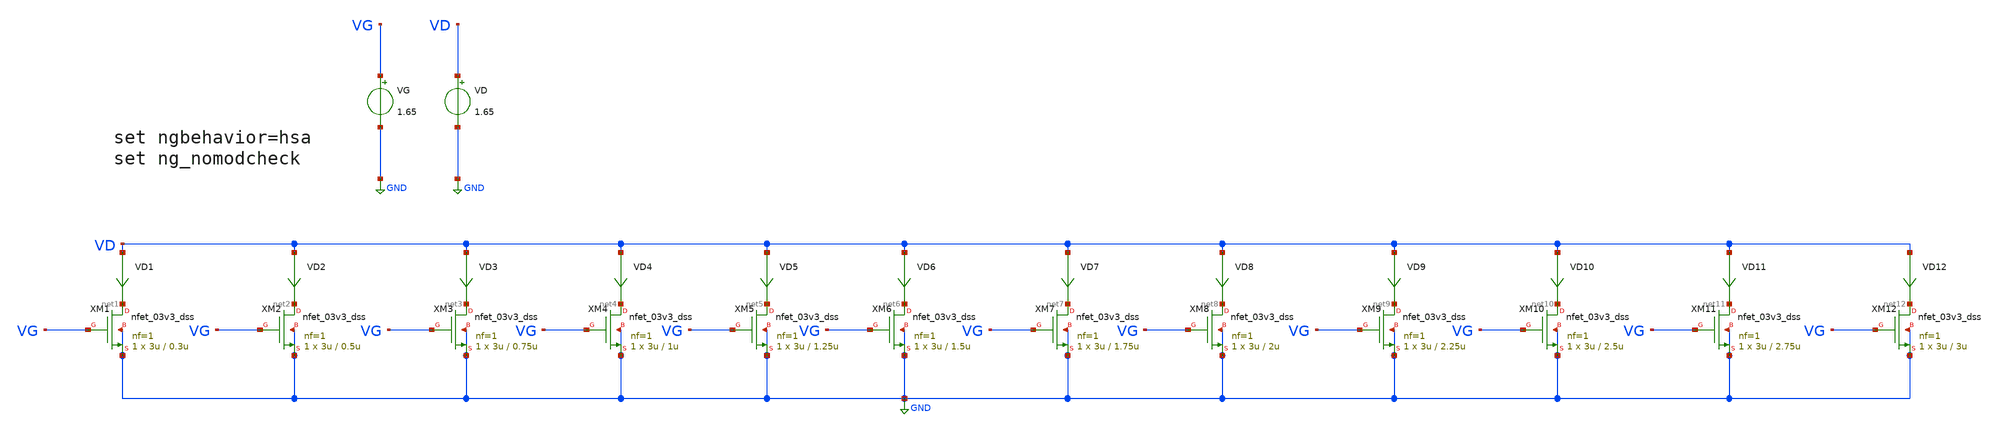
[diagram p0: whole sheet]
** sch_path: Design-Files/gmid_nmos_03v3_dss.sch
**.subckt gmid_nmos_03v3_dss
VG VG GND 1.65
VD VD GND 1.65
VD1 VD net1 0
.save i(vd1)
VD2 VD net2 0
.save i(vd2)
VD3 VD net3 0
.save i(vd3)
VD4 VD net4 0
.save i(vd4)
VD5 VD net5 0
.save i(vd5)
VD6 VD net6 0
.save i(vd6)
VD7 VD net7 0
.save i(vd7)
VD8 VD net8 0
.save i(vd8)
VD9 VD net9 0
.save i(vd9)
VD10 VD net10 0
.save i(vd10)
VD11 VD net11 0
.save i(vd11)
VD12 VD net12 0
.save i(vd12)
XM1 net1 VG GND GND nfet_03v3_dss L=0.3u W=3u nf=1 ad='int((nf+1)/2) * W/nf * 0.18u' as='int((nf+2)/2) * W/nf * 0.18u'
+ pd='2*int((nf+1)/2) * (W/nf + 0.18u)' ps='2*int((nf+2)/2) * (W/nf + 0.18u)' nrd='0.18u / W' nrs='0.18u / W'
+ sa=0 sb=0 sd=0 m=1
XM2 net2 VG GND GND nfet_03v3_dss L=0.5u W=3u nf=1 ad='int((nf+1)/2) * W/nf * 0.18u' as='int((nf+2)/2) * W/nf * 0.18u'
+ pd='2*int((nf+1)/2) * (W/nf + 0.18u)' ps='2*int((nf+2)/2) * (W/nf + 0.18u)' nrd='0.18u / W' nrs='0.18u / W'
+ sa=0 sb=0 sd=0 m=1
XM3 net3 VG GND GND nfet_03v3_dss L=0.75u W=3u nf=1 ad='int((nf+1)/2) * W/nf * 0.18u' as='int((nf+2)/2) * W/nf * 0.18u'
+ pd='2*int((nf+1)/2) * (W/nf + 0.18u)' ps='2*int((nf+2)/2) * (W/nf + 0.18u)' nrd='0.18u / W' nrs='0.18u / W'
+ sa=0 sb=0 sd=0 m=1
XM4 net4 VG GND GND nfet_03v3_dss L=1u W=3u nf=1 ad='int((nf+1)/2) * W/nf * 0.18u' as='int((nf+2)/2) * W/nf * 0.18u'
+ pd='2*int((nf+1)/2) * (W/nf + 0.18u)' ps='2*int((nf+2)/2) * (W/nf + 0.18u)' nrd='0.18u / W' nrs='0.18u / W'
+ sa=0 sb=0 sd=0 m=1
XM5 net5 VG GND GND nfet_03v3_dss L=1.25u W=3u nf=1 ad='int((nf+1)/2) * W/nf * 0.18u' as='int((nf+2)/2) * W/nf * 0.18u'
+ pd='2*int((nf+1)/2) * (W/nf + 0.18u)' ps='2*int((nf+2)/2) * (W/nf + 0.18u)' nrd='0.18u / W' nrs='0.18u / W'
+ sa=0 sb=0 sd=0 m=1
XM6 net6 VG GND GND nfet_03v3_dss L=1.5u W=3u nf=1 ad='int((nf+1)/2) * W/nf * 0.18u' as='int((nf+2)/2) * W/nf * 0.18u'
+ pd='2*int((nf+1)/2) * (W/nf + 0.18u)' ps='2*int((nf+2)/2) * (W/nf + 0.18u)' nrd='0.18u / W' nrs='0.18u / W'
+ sa=0 sb=0 sd=0 m=1
XM7 net7 VG GND GND nfet_03v3_dss L=1.75u W=3u nf=1 ad='int((nf+1)/2) * W/nf * 0.18u' as='int((nf+2)/2) * W/nf * 0.18u'
+ pd='2*int((nf+1)/2) * (W/nf + 0.18u)' ps='2*int((nf+2)/2) * (W/nf + 0.18u)' nrd='0.18u / W' nrs='0.18u / W'
+ sa=0 sb=0 sd=0 m=1
XM8 net8 VG GND GND nfet_03v3_dss L=2u W=3u nf=1 ad='int((nf+1)/2) * W/nf * 0.18u' as='int((nf+2)/2) * W/nf * 0.18u'
+ pd='2*int((nf+1)/2) * (W/nf + 0.18u)' ps='2*int((nf+2)/2) * (W/nf + 0.18u)' nrd='0.18u / W' nrs='0.18u / W'
+ sa=0 sb=0 sd=0 m=1
XM9 net9 VG GND GND nfet_03v3_dss L=2.25u W=3u nf=1 ad='int((nf+1)/2) * W/nf * 0.18u' as='int((nf+2)/2) * W/nf * 0.18u'
+ pd='2*int((nf+1)/2) * (W/nf + 0.18u)' ps='2*int((nf+2)/2) * (W/nf + 0.18u)' nrd='0.18u / W' nrs='0.18u / W'
+ sa=0 sb=0 sd=0 m=1
XM10 net10 VG GND GND nfet_03v3_dss L=2.5u W=3u nf=1 ad='int((nf+1)/2) * W/nf * 0.18u' as='int((nf+2)/2) * W/nf * 0.18u'
+ pd='2*int((nf+1)/2) * (W/nf + 0.18u)' ps='2*int((nf+2)/2) * (W/nf + 0.18u)' nrd='0.18u / W' nrs='0.18u / W'
+ sa=0 sb=0 sd=0 m=1
XM11 net11 VG GND GND nfet_03v3_dss L=2.75u W=3u nf=1 ad='int((nf+1)/2) * W/nf * 0.18u' as='int((nf+2)/2) * W/nf * 0.18u'
+ pd='2*int((nf+1)/2) * (W/nf + 0.18u)' ps='2*int((nf+2)/2) * (W/nf + 0.18u)' nrd='0.18u / W' nrs='0.18u / W'
+ sa=0 sb=0 sd=0 m=1
XM12 net12 VG GND GND nfet_03v3_dss L=3u W=3u nf=1 ad='int((nf+1)/2) * W/nf * 0.18u' as='int((nf+2)/2) * W/nf * 0.18u'
+ pd='2*int((nf+1)/2) * (W/nf + 0.18u)' ps='2*int((nf+2)/2) * (W/nf + 0.18u)' nrd='0.18u / W' nrs='0.18u / W'
+ sa=0 sb=0 sd=0 m=1
**** begin user architecture code


* ngspice commands
.option wnflag=1
.option .savecurrents
.control
save all
dc VG 0.05 1.65 0.1m
** remove zero length vectors to prevent write errors
remzerovec
write /foss/designs/PDK-CHAR/GF180-MCUD/NMOS_03v3_DSS/gmid_nmos_03v3_dss_tb.raw

plot @m.xm1.m0[gm]
plot @m.xm2.m0[gm]
plot @m.xm3.m0[gm]
plot @m.xm4.m0[gm]
plot @m.xm5.m0[gm]
plot @m.xm6.m0[gm]
plot @m.xm7.m0[gm]
plot @m.xm8.m0[gm]
plot @m.xm9.m0[gm]
plot @m.xm10.m0[gm]
plot @m.xm11.m0[gm]
plot @m.xm12.m0[gm]

wrdata /foss/designs/PDK-CHAR/GF180-MCUD/NMOS_03v3_DSS/gmid_nmos_1_nfet_03v3_dss_tb.txt
+ @m.xm1.m0[gm] i(VD1) @m.xm1.m0[vth] @m.xm1.m0[gds] @m.xm1.m0[cgg] @m.xm1.m0[cgs] @m.xm1.m0[cgd]
wrdata /foss/designs/PDK-CHAR/GF180-MCUD/NMOS_03v3_DSS/gmid_nmos_2_nfet_03v3_dss_tb.txt
+ @m.xm2.m0[gm] i(VD2) @m.xm2.m0[vth] @m.xm2.m0[gds] @m.xm2.m0[cgg] @m.xm2.m0[cgs] @m.xm2.m0[cgd]
wrdata /foss/designs/PDK-CHAR/GF180-MCUD/NMOS_03v3_DSS/gmid_nmos_3_nfet_03v3_dss_tb.txt
+ @m.xm3.m0[gm] i(VD3) @m.xm3.m0[vth] @m.xm3.m0[gds] @m.xm3.m0[cgg] @m.xm3.m0[cgs] @m.xm3.m0[cgd]
wrdata /foss/designs/PDK-CHAR/GF180-MCUD/NMOS_03v3_DSS/gmid_nmos_4_nfet_03v3_dss_tb.txt
+ @m.xm4.m0[gm] i(VD4) @m.xm4.m0[vth] @m.xm4.m0[gds] @m.xm4.m0[cgg] @m.xm4.m0[cgs] @m.xm4.m0[cgd]
wrdata /foss/designs/PDK-CHAR/GF180-MCUD/NMOS_03v3_DSS/gmid_nmos_5_nfet_03v3_dss_tb.txt
+ @m.xm5.m0[gm] i(VD5) @m.xm5.m0[vth] @m.xm5.m0[gds] @m.xm5.m0[cgg] @m.xm5.m0[cgs] @m.xm5.m0[cgd]
wrdata /foss/designs/PDK-CHAR/GF180-MCUD/NMOS_03v3_DSS/gmid_nmos_6_nfet_03v3_dss_tb.txt
+ @m.xm6.m0[gm] i(VD6) @m.xm6.m0[vth] @m.xm6.m0[gds] @m.xm6.m0[cgg] @m.xm6.m0[cgs] @m.xm6.m0[cgd]
wrdata /foss/designs/PDK-CHAR/GF180-MCUD/NMOS_03v3_DSS/gmid_nmos_7_nfet_03v3_dss_tb.txt
+ @m.xm7.m0[gm] i(VD7) @m.xm7.m0[vth] @m.xm7.m0[gds] @m.xm7.m0[cgg] @m.xm7.m0[cgs] @m.xm7.m0[cgd]
wrdata /foss/designs/PDK-CHAR/GF180-MCUD/NMOS_03v3_DSS/gmid_nmos_8_nfet_03v3_dss_tb.txt
+ @m.xm8.m0[gm] i(VD8) @m.xm8.m0[vth] @m.xm8.m0[gds] @m.xm8.m0[cgg] @m.xm8.m0[cgs] @m.xm8.m0[cgd]
wrdata /foss/designs/PDK-CHAR/GF180-MCUD/NMOS_03v3_DSS/gmid_nmos_9_nfet_03v3_dss_tb.txt
+ @m.xm9.m0[gm] i(VD9) @m.xm9.m0[vth] @m.xm9.m0[gds] @m.xm9.m0[cgg] @m.xm9.m0[cgs] @m.xm9.m0[cgd]
wrdata /foss/designs/PDK-CHAR/GF180-MCUD/NMOS_03v3_DSS/gmid_nmos_10_nfet_03v3_dss_tb.txt
+ @m.xm10.m0[gm] i(VD10) @m.xm10.m0[vth] @m.xm10.m0[gds] @m.xm10.m0[cgg] @m.xm10.m0[cgs] @m.xm10.m0[cgd]
wrdata /foss/designs/PDK-CHAR/GF180-MCUD/NMOS_03v3_DSS/gmid_nmos_11_nfet_03v3_dss_tb.txt
+ @m.xm11.m0[gm] i(VD11) @m.xm11.m0[vth] @m.xm11.m0[gds] @m.xm11.m0[cgg] @m.xm11.m0[cgs] @m.xm11.m0[cgd]
wrdata /foss/designs/PDK-CHAR/GF180-MCUD/NMOS_03v3_DSS/gmid_nmos_12_nfet_03v3_dss_tb.txt
+ @m.xm12.m0[gm] i(VD12) @m.xm12.m0[vth] @m.xm12.m0[gds] @m.xm12.m0[cgg] @m.xm12.m0[cgs] @m.xm12.m0[cgd]
set appendwrite
op
remzerovec
write /foss/designs/PDK-CHAR/GF180-MCUD/NMOS_03v3_DSS/gmid_nmos_03v3_dss_tb.raw
**quit 0
.endc




.save @m.xm1.m0[gm]
.save @m.xm1.m0[vth]
.save @m.xm1.m0[gds]
.save @m.xm1.m0[cgg]
.save @m.xm1.m0[cgs]
.save @m.xm1.m0[cgd]
.save @m.xm2.m0[gm]
.save @m.xm2.m0[vth]
.save @m.xm2.m0[gds]
.save @m.xm2.m0[cgg]
.save @m.xm2.m0[cgs]
.save @m.xm2.m0[cgd]
.save @m.xm3.m0[gm]
.save @m.xm3.m0[vth]
.save @m.xm3.m0[gds]
.save @m.xm3.m0[cgg]
.save @m.xm3.m0[cgs]
.save @m.xm3.m0[cgd]
.save @m.xm4.m0[gm]
.save @m.xm4.m0[vth]
.save @m.xm4.m0[gds]
.save @m.xm4.m0[cgg]
.save @m.xm4.m0[cgs]
.save @m.xm4.m0[cgd]
.save @m.xm5.m0[gm]
.save @m.xm5.m0[vth]
.save @m.xm5.m0[gds]
.save @m.xm5.m0[cgg]
.save @m.xm5.m0[cgs]
.save @m.xm5.m0[cgd]
.save @m.xm6.m0[gm]
.save @m.xm6.m0[vth]
.save @m.xm6.m0[gds]
.save @m.xm6.m0[cgg]
.save @m.xm6.m0[cgs]
.save @m.xm6.m0[cgd]
.save @m.xm7.m0[gm]
.save @m.xm7.m0[vth]
.save @m.xm7.m0[gds]
.save @m.xm7.m0[cgg]
.save @m.xm7.m0[cgs]
.save @m.xm7.m0[cgd]
.save @m.xm8.m0[gm]
.save @m.xm8.m0[vth]
.save @m.xm8.m0[gds]
.save @m.xm8.m0[cgg]
.save @m.xm8.m0[cgs]
.save @m.xm8.m0[cgd]
.save @m.xm9.m0[gm]
.save @m.xm9.m0[vth]
.save @m.xm9.m0[gds]
.save @m.xm9.m0[cgg]
.save @m.xm9.m0[cgs]
.save @m.xm9.m0[cgd]
.save @m.xm10.m0[gm]
.save @m.xm10.m0[vth]
.save @m.xm10.m0[gds]
.save @m.xm10.m0[cgg]
.save @m.xm10.m0[cgs]
.save @m.xm10.m0[cgd]
.save @m.xm11.m0[gm]
.save @m.xm11.m0[vth]
.save @m.xm11.m0[gds]
.save @m.xm11.m0[cgg]
.save @m.xm11.m0[cgs]
.save @m.xm11.m0[cgd]
.save @m.xm12.m0[gm]
.save @m.xm12.m0[vth]
.save @m.xm12.m0[gds]
.save @m.xm12.m0[cgg]
.save @m.xm12.m0[cgs]
.save @m.xm12.m0[cgd]




.lib /foss/pdks/volare/gf180mcu/versions/0fe599b2afb6708d281543108caf8310912f54af/gf180mcuD/libs.tech/ngspice/sm141064.ngspice typical
.include /foss/pdks/volare/gf180mcu/versions/0fe599b2afb6708d281543108caf8310912f54af/gf180mcuD/libs.tech/ngspice/design.ngspice

*.include $::180MCU_MODELS/design.ngspice
*.lib $::180MCU_MODELS/sm141064.ngspice typical


**** end user architecture code
**.ends
.GLOBAL GND
.end
